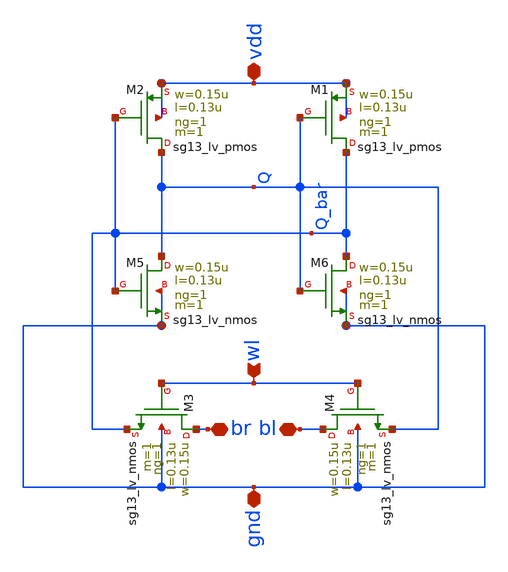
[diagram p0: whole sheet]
** sch_path: xschem/cell_1rw.sch
**.subckt cell_1rw bl br wl vdd gnd
*.iopin bl
*.iopin br
*.ipin wl
*.iopin vdd
*.iopin gnd
XM1 Q_bar Q vdd vdd sg13_lv_pmos w=0.15u l=0.13u ng=1 m=1 mm_ok=1
XM2 Q Q_bar vdd vdd sg13_lv_pmos w=0.15u l=0.13u ng=1 m=1 mm_ok=1
XM3 br wl Q_bar gnd sg13_lv_nmos w=0.15u l=0.13u ng=1 m=1 mm_ok=1
XM4 bl wl Q gnd sg13_lv_nmos w=0.15u l=0.13u ng=1 m=1 mm_ok=1
XM5 Q Q_bar gnd gnd sg13_lv_nmos w=0.15u l=0.13u ng=1 m=1 mm_ok=1
XM6 Q_bar Q gnd gnd sg13_lv_nmos w=0.15u l=0.13u ng=1 m=1 mm_ok=1
**.ends
.end
